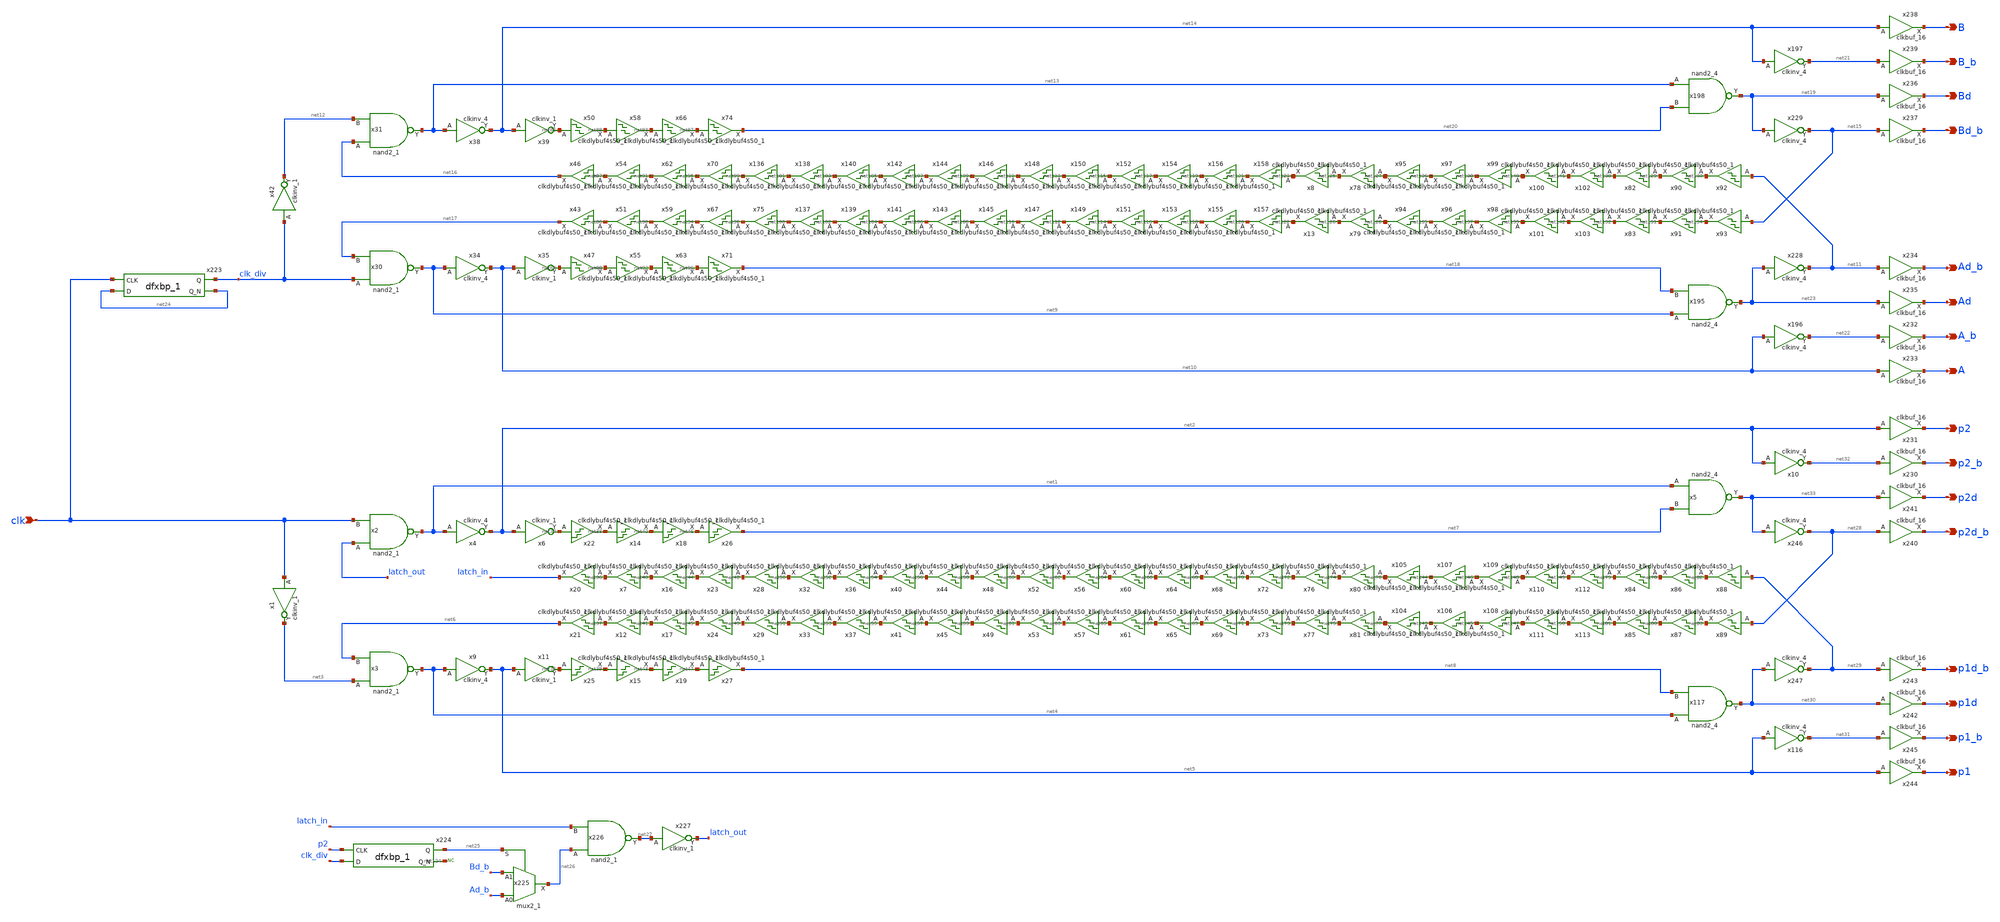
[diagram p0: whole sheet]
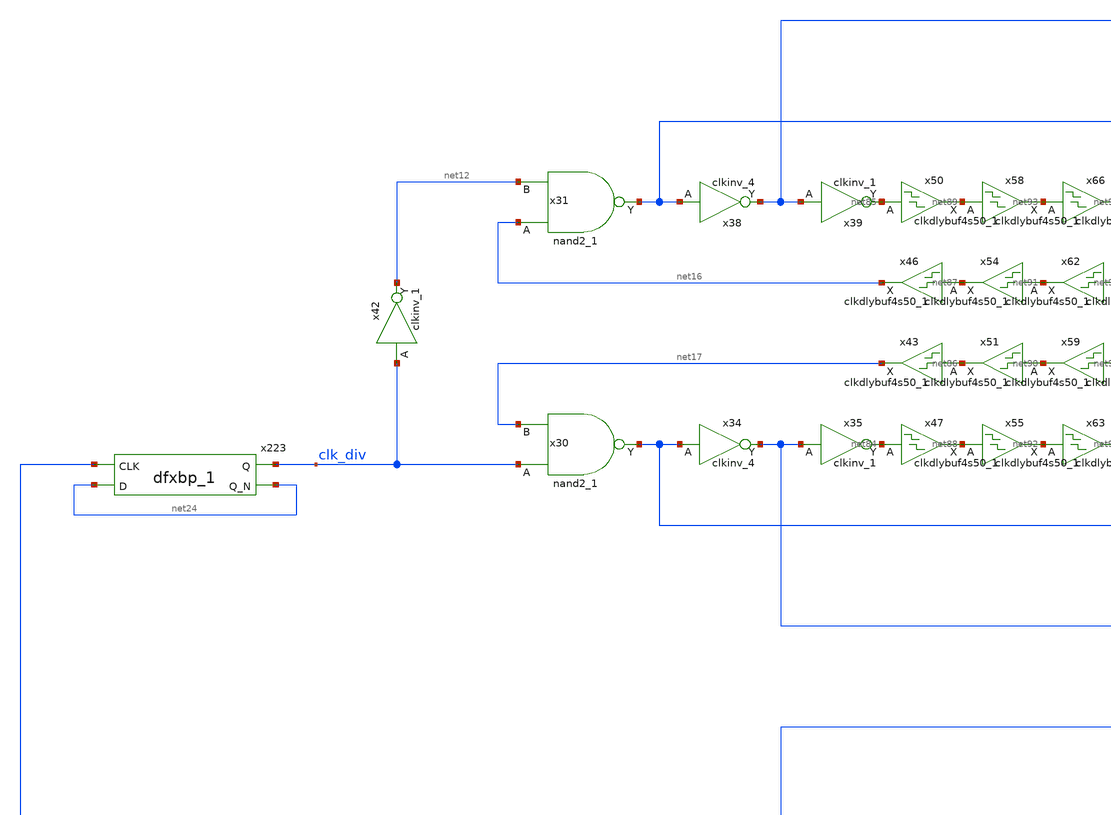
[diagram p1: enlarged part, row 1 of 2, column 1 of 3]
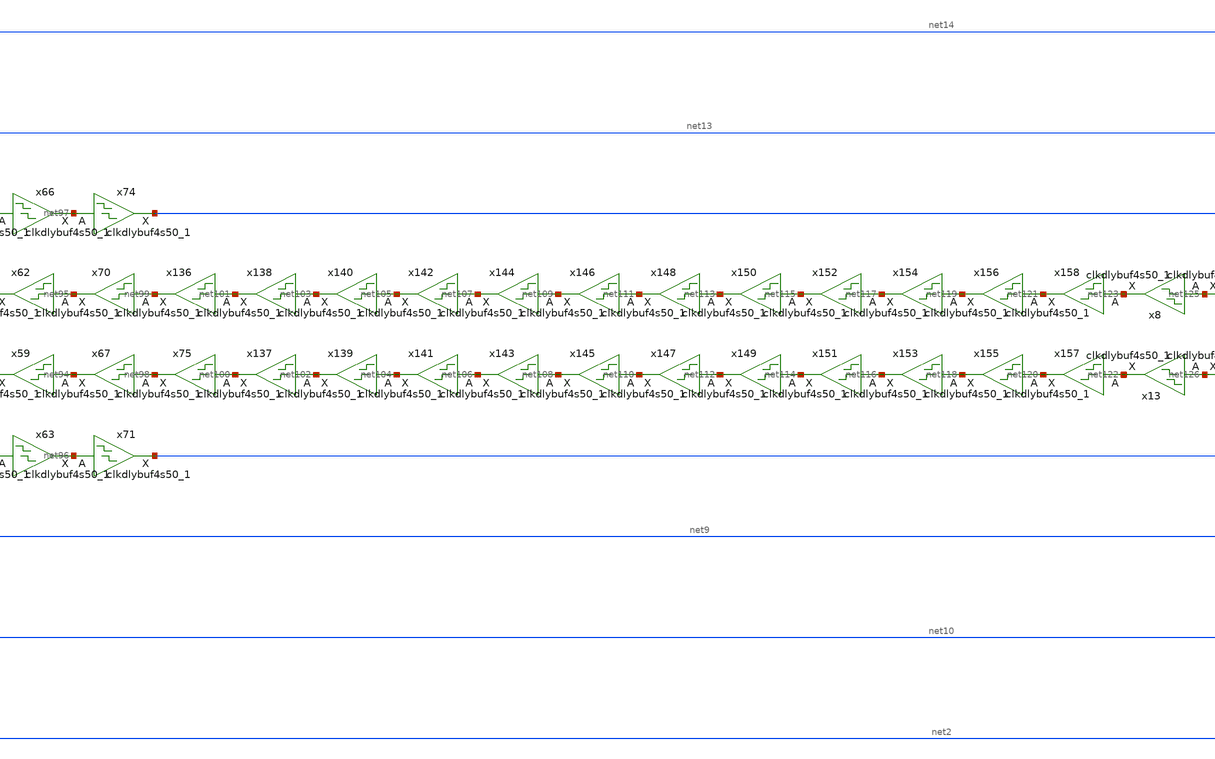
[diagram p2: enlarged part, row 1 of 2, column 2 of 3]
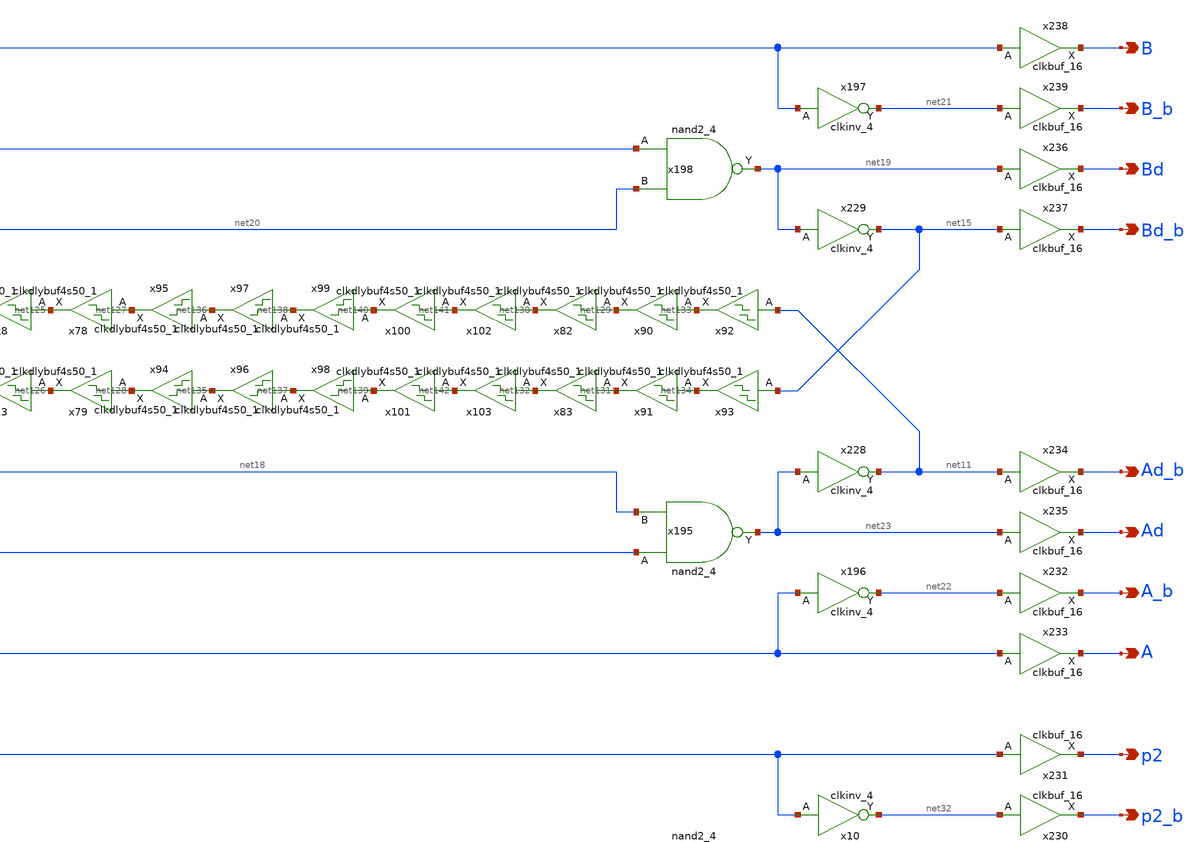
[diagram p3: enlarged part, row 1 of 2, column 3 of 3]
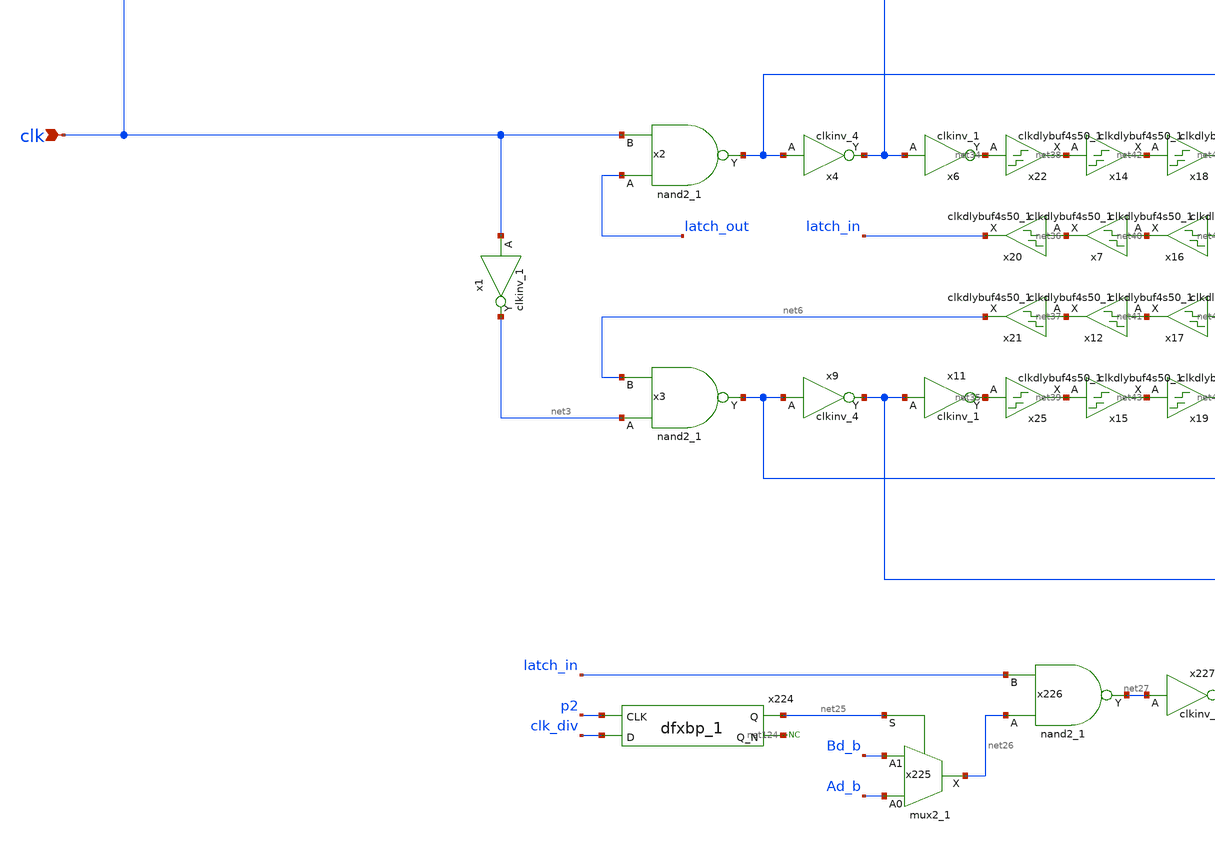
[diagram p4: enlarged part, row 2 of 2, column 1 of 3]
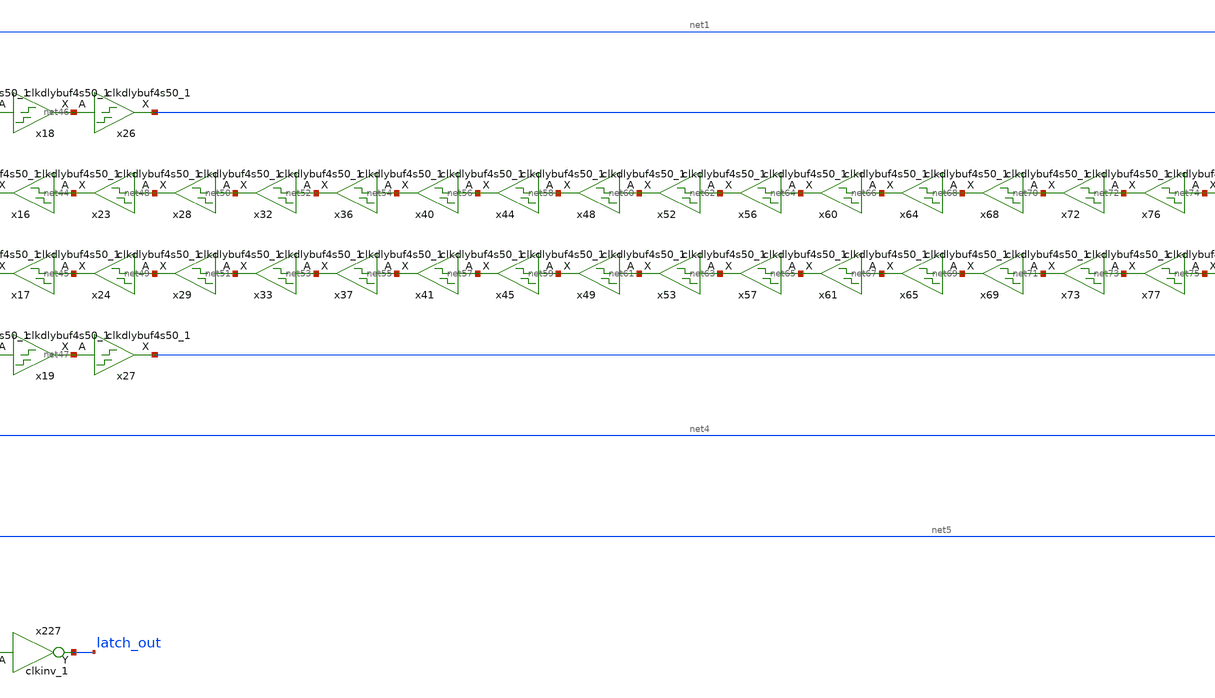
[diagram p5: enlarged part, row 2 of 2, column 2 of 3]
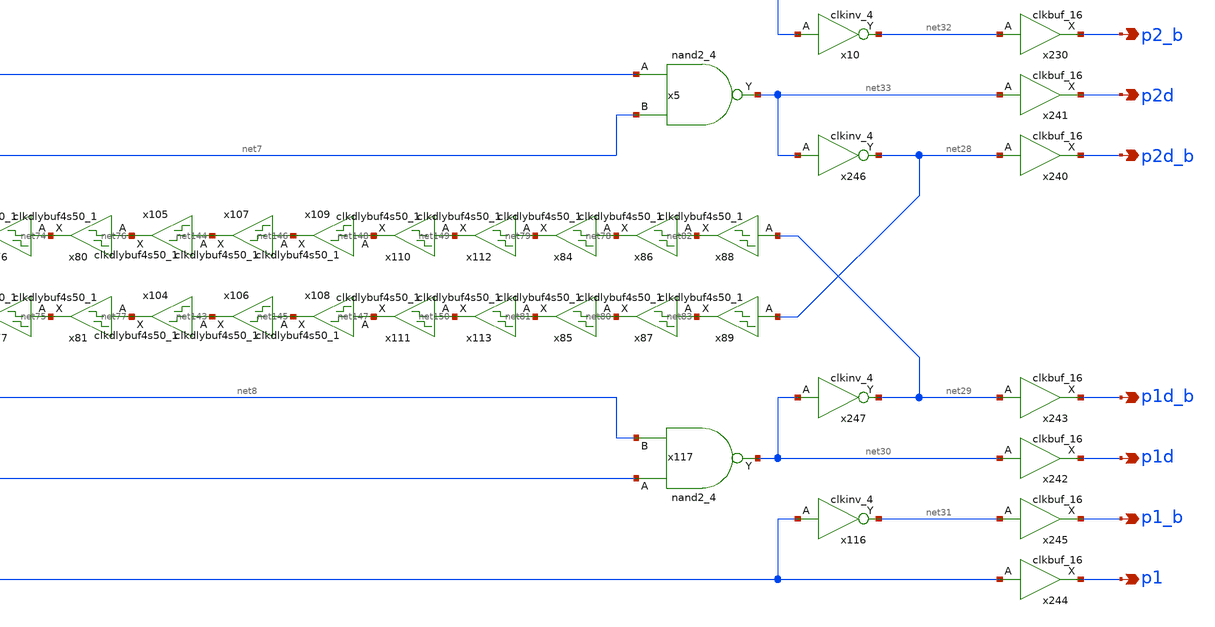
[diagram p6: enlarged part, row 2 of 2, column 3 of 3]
** sch_path: design/analog_modulator/schematic/clock_v2.sch
**.subckt clock_v2 clk p2d_b p2d p2_b p2 p1d_b p1d p1_b p1 Ad_b Ad A_b A Bd_b Bd B_b B
*.ipin clk
*.opin p2d_b
*.opin p2d
*.opin p2_b
*.opin p2
*.opin p1d_b
*.opin p1d
*.opin p1_b
*.opin p1
*.opin Ad_b
*.opin Ad
*.opin A_b
*.opin A
*.opin Bd_b
*.opin Bd
*.opin B_b
*.opin B
x2 latch_out clk VSS VSS VDD VDD net1 sky130_fd_sc_hd__nand2_1
x3 net3 net6 VSS VSS VDD VDD net4 sky130_fd_sc_hd__nand2_1
x4 net1 VSS VSS VDD VDD net2 sky130_fd_sc_hd__clkinv_4
x6 net2 VSS VSS VDD VDD net34 sky130_fd_sc_hd__clkinv_1
x9 net4 VSS VSS VDD VDD net5 sky130_fd_sc_hd__clkinv_4
x11 net5 VSS VSS VDD VDD net35 sky130_fd_sc_hd__clkinv_1
x1 clk VSS VSS VDD VDD net3 sky130_fd_sc_hd__clkinv_1
x20 net36 VSS VSS VDD VDD latch_in sky130_fd_sc_hd__clkdlybuf4s50_1
x21 net37 VSS VSS VDD VDD net6 sky130_fd_sc_hd__clkdlybuf4s50_1
x22 net34 VSS VSS VDD VDD net38 sky130_fd_sc_hd__clkdlybuf4s50_1
x25 net35 VSS VSS VDD VDD net39 sky130_fd_sc_hd__clkdlybuf4s50_1
x7 net40 VSS VSS VDD VDD net36 sky130_fd_sc_hd__clkdlybuf4s50_1
x12 net41 VSS VSS VDD VDD net37 sky130_fd_sc_hd__clkdlybuf4s50_1
x14 net38 VSS VSS VDD VDD net42 sky130_fd_sc_hd__clkdlybuf4s50_1
x15 net39 VSS VSS VDD VDD net43 sky130_fd_sc_hd__clkdlybuf4s50_1
x16 net44 VSS VSS VDD VDD net40 sky130_fd_sc_hd__clkdlybuf4s50_1
x17 net45 VSS VSS VDD VDD net41 sky130_fd_sc_hd__clkdlybuf4s50_1
x18 net42 VSS VSS VDD VDD net46 sky130_fd_sc_hd__clkdlybuf4s50_1
x19 net43 VSS VSS VDD VDD net47 sky130_fd_sc_hd__clkdlybuf4s50_1
x23 net48 VSS VSS VDD VDD net44 sky130_fd_sc_hd__clkdlybuf4s50_1
x24 net49 VSS VSS VDD VDD net45 sky130_fd_sc_hd__clkdlybuf4s50_1
x26 net46 VSS VSS VDD VDD net7 sky130_fd_sc_hd__clkdlybuf4s50_1
x27 net47 VSS VSS VDD VDD net8 sky130_fd_sc_hd__clkdlybuf4s50_1
x28 net50 VSS VSS VDD VDD net48 sky130_fd_sc_hd__clkdlybuf4s50_1
x29 net51 VSS VSS VDD VDD net49 sky130_fd_sc_hd__clkdlybuf4s50_1
x32 net52 VSS VSS VDD VDD net50 sky130_fd_sc_hd__clkdlybuf4s50_1
x33 net53 VSS VSS VDD VDD net51 sky130_fd_sc_hd__clkdlybuf4s50_1
x36 net54 VSS VSS VDD VDD net52 sky130_fd_sc_hd__clkdlybuf4s50_1
x37 net55 VSS VSS VDD VDD net53 sky130_fd_sc_hd__clkdlybuf4s50_1
x40 net56 VSS VSS VDD VDD net54 sky130_fd_sc_hd__clkdlybuf4s50_1
x41 net57 VSS VSS VDD VDD net55 sky130_fd_sc_hd__clkdlybuf4s50_1
x44 net58 VSS VSS VDD VDD net56 sky130_fd_sc_hd__clkdlybuf4s50_1
x45 net59 VSS VSS VDD VDD net57 sky130_fd_sc_hd__clkdlybuf4s50_1
x48 net60 VSS VSS VDD VDD net58 sky130_fd_sc_hd__clkdlybuf4s50_1
x49 net61 VSS VSS VDD VDD net59 sky130_fd_sc_hd__clkdlybuf4s50_1
x52 net62 VSS VSS VDD VDD net60 sky130_fd_sc_hd__clkdlybuf4s50_1
x53 net63 VSS VSS VDD VDD net61 sky130_fd_sc_hd__clkdlybuf4s50_1
x56 net64 VSS VSS VDD VDD net62 sky130_fd_sc_hd__clkdlybuf4s50_1
x57 net65 VSS VSS VDD VDD net63 sky130_fd_sc_hd__clkdlybuf4s50_1
x60 net66 VSS VSS VDD VDD net64 sky130_fd_sc_hd__clkdlybuf4s50_1
x61 net67 VSS VSS VDD VDD net65 sky130_fd_sc_hd__clkdlybuf4s50_1
x64 net68 VSS VSS VDD VDD net66 sky130_fd_sc_hd__clkdlybuf4s50_1
x65 net69 VSS VSS VDD VDD net67 sky130_fd_sc_hd__clkdlybuf4s50_1
x68 net70 VSS VSS VDD VDD net68 sky130_fd_sc_hd__clkdlybuf4s50_1
x69 net71 VSS VSS VDD VDD net69 sky130_fd_sc_hd__clkdlybuf4s50_1
x72 net72 VSS VSS VDD VDD net70 sky130_fd_sc_hd__clkdlybuf4s50_1
x73 net73 VSS VSS VDD VDD net71 sky130_fd_sc_hd__clkdlybuf4s50_1
x76 net74 VSS VSS VDD VDD net72 sky130_fd_sc_hd__clkdlybuf4s50_1
x77 net75 VSS VSS VDD VDD net73 sky130_fd_sc_hd__clkdlybuf4s50_1
x80 net76 VSS VSS VDD VDD net74 sky130_fd_sc_hd__clkdlybuf4s50_1
x81 net77 VSS VSS VDD VDD net75 sky130_fd_sc_hd__clkdlybuf4s50_1
x84 net78 VSS VSS VDD VDD net79 sky130_fd_sc_hd__clkdlybuf4s50_1
x85 net80 VSS VSS VDD VDD net81 sky130_fd_sc_hd__clkdlybuf4s50_1
x86 net82 VSS VSS VDD VDD net78 sky130_fd_sc_hd__clkdlybuf4s50_1
x87 net83 VSS VSS VDD VDD net80 sky130_fd_sc_hd__clkdlybuf4s50_1
x88 net29 VSS VSS VDD VDD net82 sky130_fd_sc_hd__clkdlybuf4s50_1
x89 net28 VSS VSS VDD VDD net83 sky130_fd_sc_hd__clkdlybuf4s50_1
x30 clk_div net17 VSS VSS VDD VDD net9 sky130_fd_sc_hd__nand2_1
x31 net16 net12 VSS VSS VDD VDD net13 sky130_fd_sc_hd__nand2_1
x34 net9 VSS VSS VDD VDD net10 sky130_fd_sc_hd__clkinv_4
x35 net10 VSS VSS VDD VDD net84 sky130_fd_sc_hd__clkinv_1
x38 net13 VSS VSS VDD VDD net14 sky130_fd_sc_hd__clkinv_4
x39 net14 VSS VSS VDD VDD net85 sky130_fd_sc_hd__clkinv_1
x42 clk_div VSS VSS VDD VDD net12 sky130_fd_sc_hd__clkinv_1
x43 net86 VSS VSS VDD VDD net17 sky130_fd_sc_hd__clkdlybuf4s50_1
x46 net87 VSS VSS VDD VDD net16 sky130_fd_sc_hd__clkdlybuf4s50_1
x47 net84 VSS VSS VDD VDD net88 sky130_fd_sc_hd__clkdlybuf4s50_1
x50 net85 VSS VSS VDD VDD net89 sky130_fd_sc_hd__clkdlybuf4s50_1
x51 net90 VSS VSS VDD VDD net86 sky130_fd_sc_hd__clkdlybuf4s50_1
x54 net91 VSS VSS VDD VDD net87 sky130_fd_sc_hd__clkdlybuf4s50_1
x55 net88 VSS VSS VDD VDD net92 sky130_fd_sc_hd__clkdlybuf4s50_1
x58 net89 VSS VSS VDD VDD net93 sky130_fd_sc_hd__clkdlybuf4s50_1
x59 net94 VSS VSS VDD VDD net90 sky130_fd_sc_hd__clkdlybuf4s50_1
x62 net95 VSS VSS VDD VDD net91 sky130_fd_sc_hd__clkdlybuf4s50_1
x63 net92 VSS VSS VDD VDD net96 sky130_fd_sc_hd__clkdlybuf4s50_1
x66 net93 VSS VSS VDD VDD net97 sky130_fd_sc_hd__clkdlybuf4s50_1
x67 net98 VSS VSS VDD VDD net94 sky130_fd_sc_hd__clkdlybuf4s50_1
x70 net99 VSS VSS VDD VDD net95 sky130_fd_sc_hd__clkdlybuf4s50_1
x71 net96 VSS VSS VDD VDD net18 sky130_fd_sc_hd__clkdlybuf4s50_1
x74 net97 VSS VSS VDD VDD net20 sky130_fd_sc_hd__clkdlybuf4s50_1
x75 net100 VSS VSS VDD VDD net98 sky130_fd_sc_hd__clkdlybuf4s50_1
x136 net101 VSS VSS VDD VDD net99 sky130_fd_sc_hd__clkdlybuf4s50_1
x137 net102 VSS VSS VDD VDD net100 sky130_fd_sc_hd__clkdlybuf4s50_1
x138 net103 VSS VSS VDD VDD net101 sky130_fd_sc_hd__clkdlybuf4s50_1
x139 net104 VSS VSS VDD VDD net102 sky130_fd_sc_hd__clkdlybuf4s50_1
x140 net105 VSS VSS VDD VDD net103 sky130_fd_sc_hd__clkdlybuf4s50_1
x141 net106 VSS VSS VDD VDD net104 sky130_fd_sc_hd__clkdlybuf4s50_1
x142 net107 VSS VSS VDD VDD net105 sky130_fd_sc_hd__clkdlybuf4s50_1
x143 net108 VSS VSS VDD VDD net106 sky130_fd_sc_hd__clkdlybuf4s50_1
x144 net109 VSS VSS VDD VDD net107 sky130_fd_sc_hd__clkdlybuf4s50_1
x145 net110 VSS VSS VDD VDD net108 sky130_fd_sc_hd__clkdlybuf4s50_1
x146 net111 VSS VSS VDD VDD net109 sky130_fd_sc_hd__clkdlybuf4s50_1
x147 net112 VSS VSS VDD VDD net110 sky130_fd_sc_hd__clkdlybuf4s50_1
x148 net113 VSS VSS VDD VDD net111 sky130_fd_sc_hd__clkdlybuf4s50_1
x149 net114 VSS VSS VDD VDD net112 sky130_fd_sc_hd__clkdlybuf4s50_1
x150 net115 VSS VSS VDD VDD net113 sky130_fd_sc_hd__clkdlybuf4s50_1
x151 net116 VSS VSS VDD VDD net114 sky130_fd_sc_hd__clkdlybuf4s50_1
x152 net117 VSS VSS VDD VDD net115 sky130_fd_sc_hd__clkdlybuf4s50_1
x153 net118 VSS VSS VDD VDD net116 sky130_fd_sc_hd__clkdlybuf4s50_1
x154 net119 VSS VSS VDD VDD net117 sky130_fd_sc_hd__clkdlybuf4s50_1
x155 net120 VSS VSS VDD VDD net118 sky130_fd_sc_hd__clkdlybuf4s50_1
x156 net121 VSS VSS VDD VDD net119 sky130_fd_sc_hd__clkdlybuf4s50_1
x157 net122 VSS VSS VDD VDD net120 sky130_fd_sc_hd__clkdlybuf4s50_1
x158 net123 VSS VSS VDD VDD net121 sky130_fd_sc_hd__clkdlybuf4s50_1
x195 net9 net18 VSS VSS VDD VDD net23 sky130_fd_sc_hd__nand2_4
x196 net10 VSS VSS VDD VDD net22 sky130_fd_sc_hd__clkinv_4
x197 net14 VSS VSS VDD VDD net21 sky130_fd_sc_hd__clkinv_4
x198 net13 net20 VSS VSS VDD VDD net19 sky130_fd_sc_hd__nand2_4
x223 clk net24 VSS VSS VDD VDD clk_div net24 sky130_fd_sc_hd__dfxbp_1
x224 p2 clk_div VSS VSS VDD VDD net25 net124 sky130_fd_sc_hd__dfxbp_1
x225 Ad_b Bd_b net25 VSS VSS VDD VDD net26 sky130_fd_sc_hd__mux2_1
x226 net26 latch_in VSS VSS VDD VDD net27 sky130_fd_sc_hd__nand2_1
x227 net27 VSS VSS VDD VDD latch_out sky130_fd_sc_hd__clkinv_1
* noconn #net124
x232 net22 VSS VSS VDD VDD A_b sky130_fd_sc_hd__clkbuf_16
x233 net10 VSS VSS VDD VDD A sky130_fd_sc_hd__clkbuf_16
x234 net11 VSS VSS VDD VDD Ad_b sky130_fd_sc_hd__clkbuf_16
x235 net23 VSS VSS VDD VDD Ad sky130_fd_sc_hd__clkbuf_16
x236 net19 VSS VSS VDD VDD Bd sky130_fd_sc_hd__clkbuf_16
x237 net15 VSS VSS VDD VDD Bd_b sky130_fd_sc_hd__clkbuf_16
x238 net14 VSS VSS VDD VDD B sky130_fd_sc_hd__clkbuf_16
x239 net21 VSS VSS VDD VDD B_b sky130_fd_sc_hd__clkbuf_16
x228 net23 VSS VSS VDD VDD net11 sky130_fd_sc_hd__clkinv_4
x229 net19 VSS VSS VDD VDD net15 sky130_fd_sc_hd__clkinv_4
x5 net1 net7 VSS VSS VDD VDD net33 sky130_fd_sc_hd__nand2_4
x10 net2 VSS VSS VDD VDD net32 sky130_fd_sc_hd__clkinv_4
x116 net5 VSS VSS VDD VDD net31 sky130_fd_sc_hd__clkinv_4
x117 net4 net8 VSS VSS VDD VDD net30 sky130_fd_sc_hd__nand2_4
x230 net32 VSS VSS VDD VDD p2_b sky130_fd_sc_hd__clkbuf_16
x231 net2 VSS VSS VDD VDD p2 sky130_fd_sc_hd__clkbuf_16
x240 net28 VSS VSS VDD VDD p2d_b sky130_fd_sc_hd__clkbuf_16
x241 net33 VSS VSS VDD VDD p2d sky130_fd_sc_hd__clkbuf_16
x242 net30 VSS VSS VDD VDD p1d sky130_fd_sc_hd__clkbuf_16
x243 net29 VSS VSS VDD VDD p1d_b sky130_fd_sc_hd__clkbuf_16
x244 net5 VSS VSS VDD VDD p1 sky130_fd_sc_hd__clkbuf_16
x245 net31 VSS VSS VDD VDD p1_b sky130_fd_sc_hd__clkbuf_16
x246 net33 VSS VSS VDD VDD net28 sky130_fd_sc_hd__clkinv_4
x247 net30 VSS VSS VDD VDD net29 sky130_fd_sc_hd__clkinv_4
x8 net125 VSS VSS VDD VDD net123 sky130_fd_sc_hd__clkdlybuf4s50_1
x13 net126 VSS VSS VDD VDD net122 sky130_fd_sc_hd__clkdlybuf4s50_1
x78 net127 VSS VSS VDD VDD net125 sky130_fd_sc_hd__clkdlybuf4s50_1
x79 net128 VSS VSS VDD VDD net126 sky130_fd_sc_hd__clkdlybuf4s50_1
x82 net129 VSS VSS VDD VDD net130 sky130_fd_sc_hd__clkdlybuf4s50_1
x83 net131 VSS VSS VDD VDD net132 sky130_fd_sc_hd__clkdlybuf4s50_1
x90 net133 VSS VSS VDD VDD net129 sky130_fd_sc_hd__clkdlybuf4s50_1
x91 net134 VSS VSS VDD VDD net131 sky130_fd_sc_hd__clkdlybuf4s50_1
x92 net11 VSS VSS VDD VDD net133 sky130_fd_sc_hd__clkdlybuf4s50_1
x93 net15 VSS VSS VDD VDD net134 sky130_fd_sc_hd__clkdlybuf4s50_1
x94 net135 VSS VSS VDD VDD net128 sky130_fd_sc_hd__clkdlybuf4s50_1
x95 net136 VSS VSS VDD VDD net127 sky130_fd_sc_hd__clkdlybuf4s50_1
x96 net137 VSS VSS VDD VDD net135 sky130_fd_sc_hd__clkdlybuf4s50_1
x97 net138 VSS VSS VDD VDD net136 sky130_fd_sc_hd__clkdlybuf4s50_1
x98 net139 VSS VSS VDD VDD net137 sky130_fd_sc_hd__clkdlybuf4s50_1
x99 net140 VSS VSS VDD VDD net138 sky130_fd_sc_hd__clkdlybuf4s50_1
x100 net141 VSS VSS VDD VDD net140 sky130_fd_sc_hd__clkdlybuf4s50_1
x101 net142 VSS VSS VDD VDD net139 sky130_fd_sc_hd__clkdlybuf4s50_1
x102 net130 VSS VSS VDD VDD net141 sky130_fd_sc_hd__clkdlybuf4s50_1
x103 net132 VSS VSS VDD VDD net142 sky130_fd_sc_hd__clkdlybuf4s50_1
x104 net143 VSS VSS VDD VDD net77 sky130_fd_sc_hd__clkdlybuf4s50_1
x105 net144 VSS VSS VDD VDD net76 sky130_fd_sc_hd__clkdlybuf4s50_1
x106 net145 VSS VSS VDD VDD net143 sky130_fd_sc_hd__clkdlybuf4s50_1
x107 net146 VSS VSS VDD VDD net144 sky130_fd_sc_hd__clkdlybuf4s50_1
x108 net147 VSS VSS VDD VDD net145 sky130_fd_sc_hd__clkdlybuf4s50_1
x109 net148 VSS VSS VDD VDD net146 sky130_fd_sc_hd__clkdlybuf4s50_1
x110 net149 VSS VSS VDD VDD net148 sky130_fd_sc_hd__clkdlybuf4s50_1
x111 net150 VSS VSS VDD VDD net147 sky130_fd_sc_hd__clkdlybuf4s50_1
x112 net79 VSS VSS VDD VDD net149 sky130_fd_sc_hd__clkdlybuf4s50_1
x113 net81 VSS VSS VDD VDD net150 sky130_fd_sc_hd__clkdlybuf4s50_1
**.ends
.end
